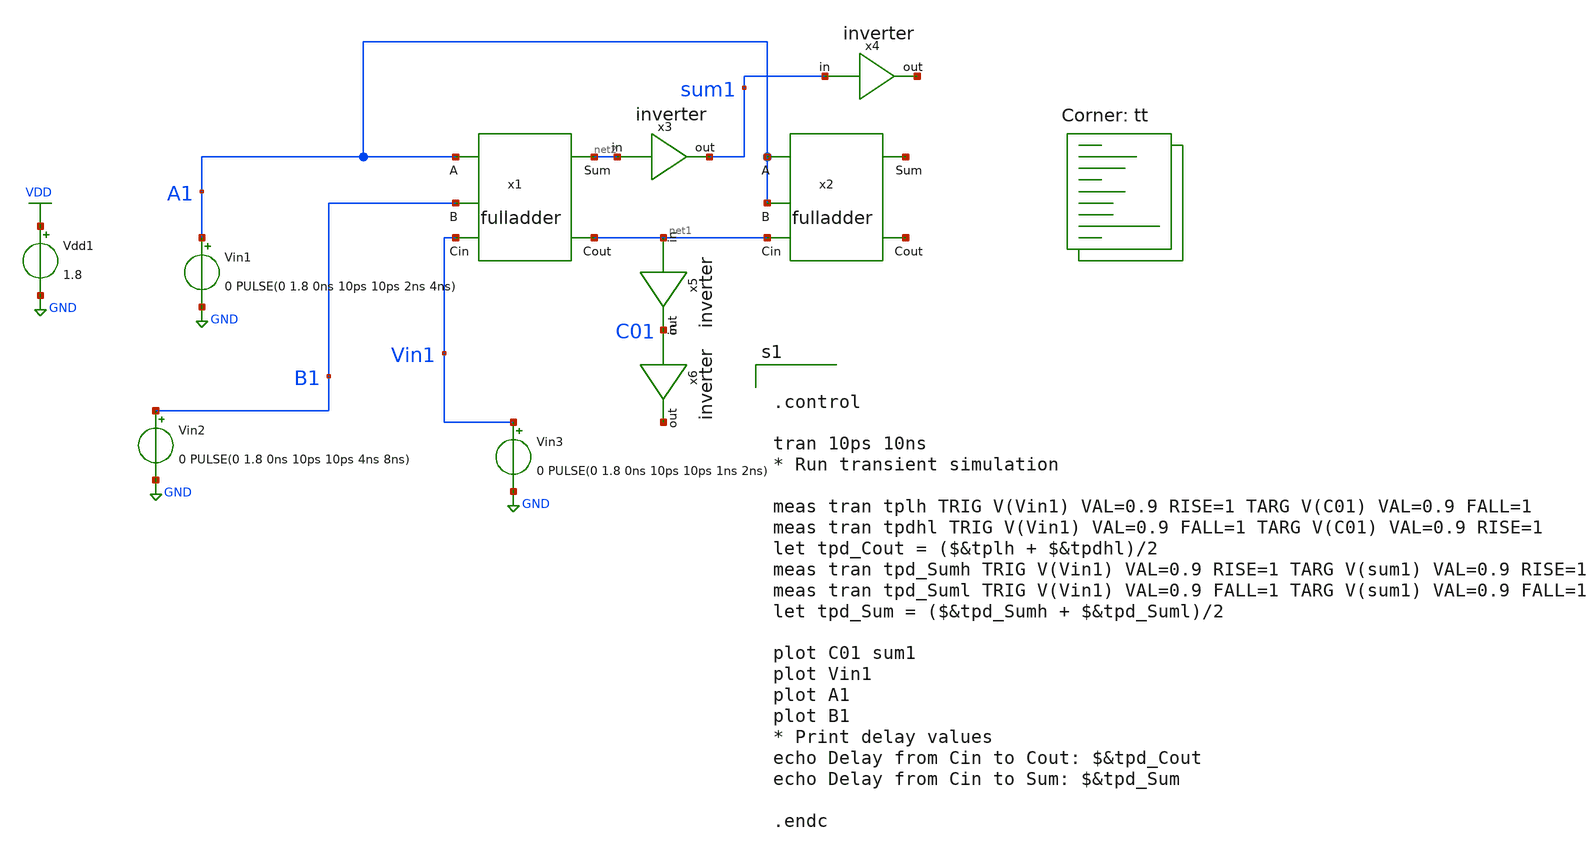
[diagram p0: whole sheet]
** sch_path: Tutorial_6/rippleadder.sch
**.subckt rippleadder
x1 A1 B1 Vin1 net1 net2 fulladder
x2 A1 A1 net1 net3 net4 fulladder
x3 sum1 net2 inverter
Vdd1 VDD GND 1.8
Vin1 A1 GND 0 PULSE(0 1.8 0ns 10ps 10ps 2ns 4ns)
x4 net5 sum1 inverter
Vin2 B1 GND 0 PULSE(0 1.8 0ns 10ps 10ps 4ns 8ns)
Vin3 Vin1 GND 0 PULSE(0 1.8 0ns 10ps 10ps 1ns 2ns)
x5 C01 net1 inverter
x6 net6 C01 inverter
**** begin user architecture code


.control

tran 10ps 10ns
* Run transient simulation

meas tran tplh TRIG V(Vin1) VAL=0.9 RISE=1 TARG V(C01) VAL=0.9 FALL=1
meas tran tpdhl TRIG V(Vin1) VAL=0.9 FALL=1 TARG V(C01) VAL=0.9 RISE=1
let tpd_Cout = ($&tplh + $&tpdhl)/2
meas tran tpd_Sumh TRIG V(Vin1) VAL=0.9 RISE=1 TARG V(sum1) VAL=0.9 RISE=1
meas tran tpd_Suml TRIG V(Vin1) VAL=0.9 FALL=1 TARG V(sum1) VAL=0.9 FALL=1
let tpd_Sum = ($&tpd_Sumh + $&tpd_Suml)/2

plot C01 sum1
plot Vin1
plot A1
plot B1
* Print delay values
echo Delay from Cin to Cout: $&tpd_Cout
echo Delay from Cin to Sum: $&tpd_Sum

.endc


.lib $::SKYWATER_MODELS/sky130.lib.spice tt
**** end user architecture code
**.ends
.GLOBAL GND
.GLOBAL VDD
.end
